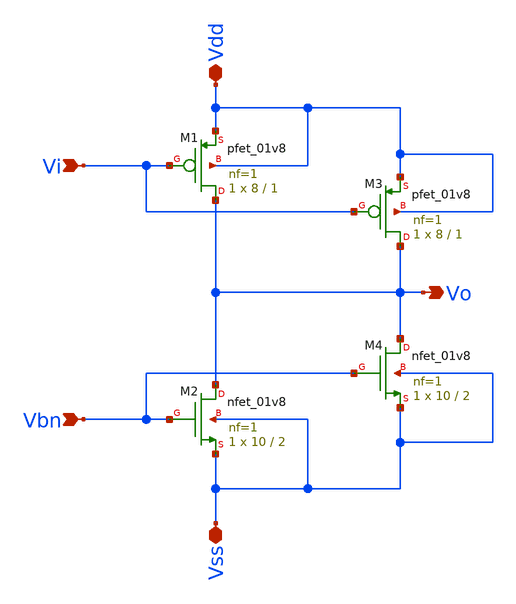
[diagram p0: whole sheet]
** sch_path: Circuits/Examples/OpAmp/CSAmp.sch
**.subckt CSAmp Vbn Vi Vdd Vss Vo
*.ipin Vbn
*.ipin Vi
*.iopin Vdd
*.iopin Vss
*.opin Vo
XM1 Vo Vi Vdd Vdd sky130_fd_pr__pfet_01v8 L=1 W=8 nf=1 ad='int((nf+1)/2) * W/nf * 0.29' as='int((nf+2)/2) * W/nf * 0.29'
+ pd='2*int((nf+1)/2) * (W/nf + 0.29)' ps='2*int((nf+2)/2) * (W/nf + 0.29)' nrd='0.29 / W' nrs='0.29 / W'
+ sa=0 sb=0 sd=0 mult=1 m=1
XM2 Vo Vbn Vss Vss sky130_fd_pr__nfet_01v8 L=2 W=10 nf=1 ad='int((nf+1)/2) * W/nf * 0.29' as='int((nf+2)/2) * W/nf * 0.29'
+ pd='2*int((nf+1)/2) * (W/nf + 0.29)' ps='2*int((nf+2)/2) * (W/nf + 0.29)' nrd='0.29 / W' nrs='0.29 / W'
+ sa=0 sb=0 sd=0 mult=1 m=1
XM3 Vo Vi Vdd Vdd sky130_fd_pr__pfet_01v8 L=1 W=8 nf=1 ad='int((nf+1)/2) * W/nf * 0.29' as='int((nf+2)/2) * W/nf * 0.29'
+ pd='2*int((nf+1)/2) * (W/nf + 0.29)' ps='2*int((nf+2)/2) * (W/nf + 0.29)' nrd='0.29 / W' nrs='0.29 / W'
+ sa=0 sb=0 sd=0 mult=1 m=1
XM4 Vo Vbn Vss Vss sky130_fd_pr__nfet_01v8 L=2 W=10 nf=1 ad='int((nf+1)/2) * W/nf * 0.29' as='int((nf+2)/2) * W/nf * 0.29'
+ pd='2*int((nf+1)/2) * (W/nf + 0.29)' ps='2*int((nf+2)/2) * (W/nf + 0.29)' nrd='0.29 / W' nrs='0.29 / W'
+ sa=0 sb=0 sd=0 mult=1 m=1
**.ends
.end
